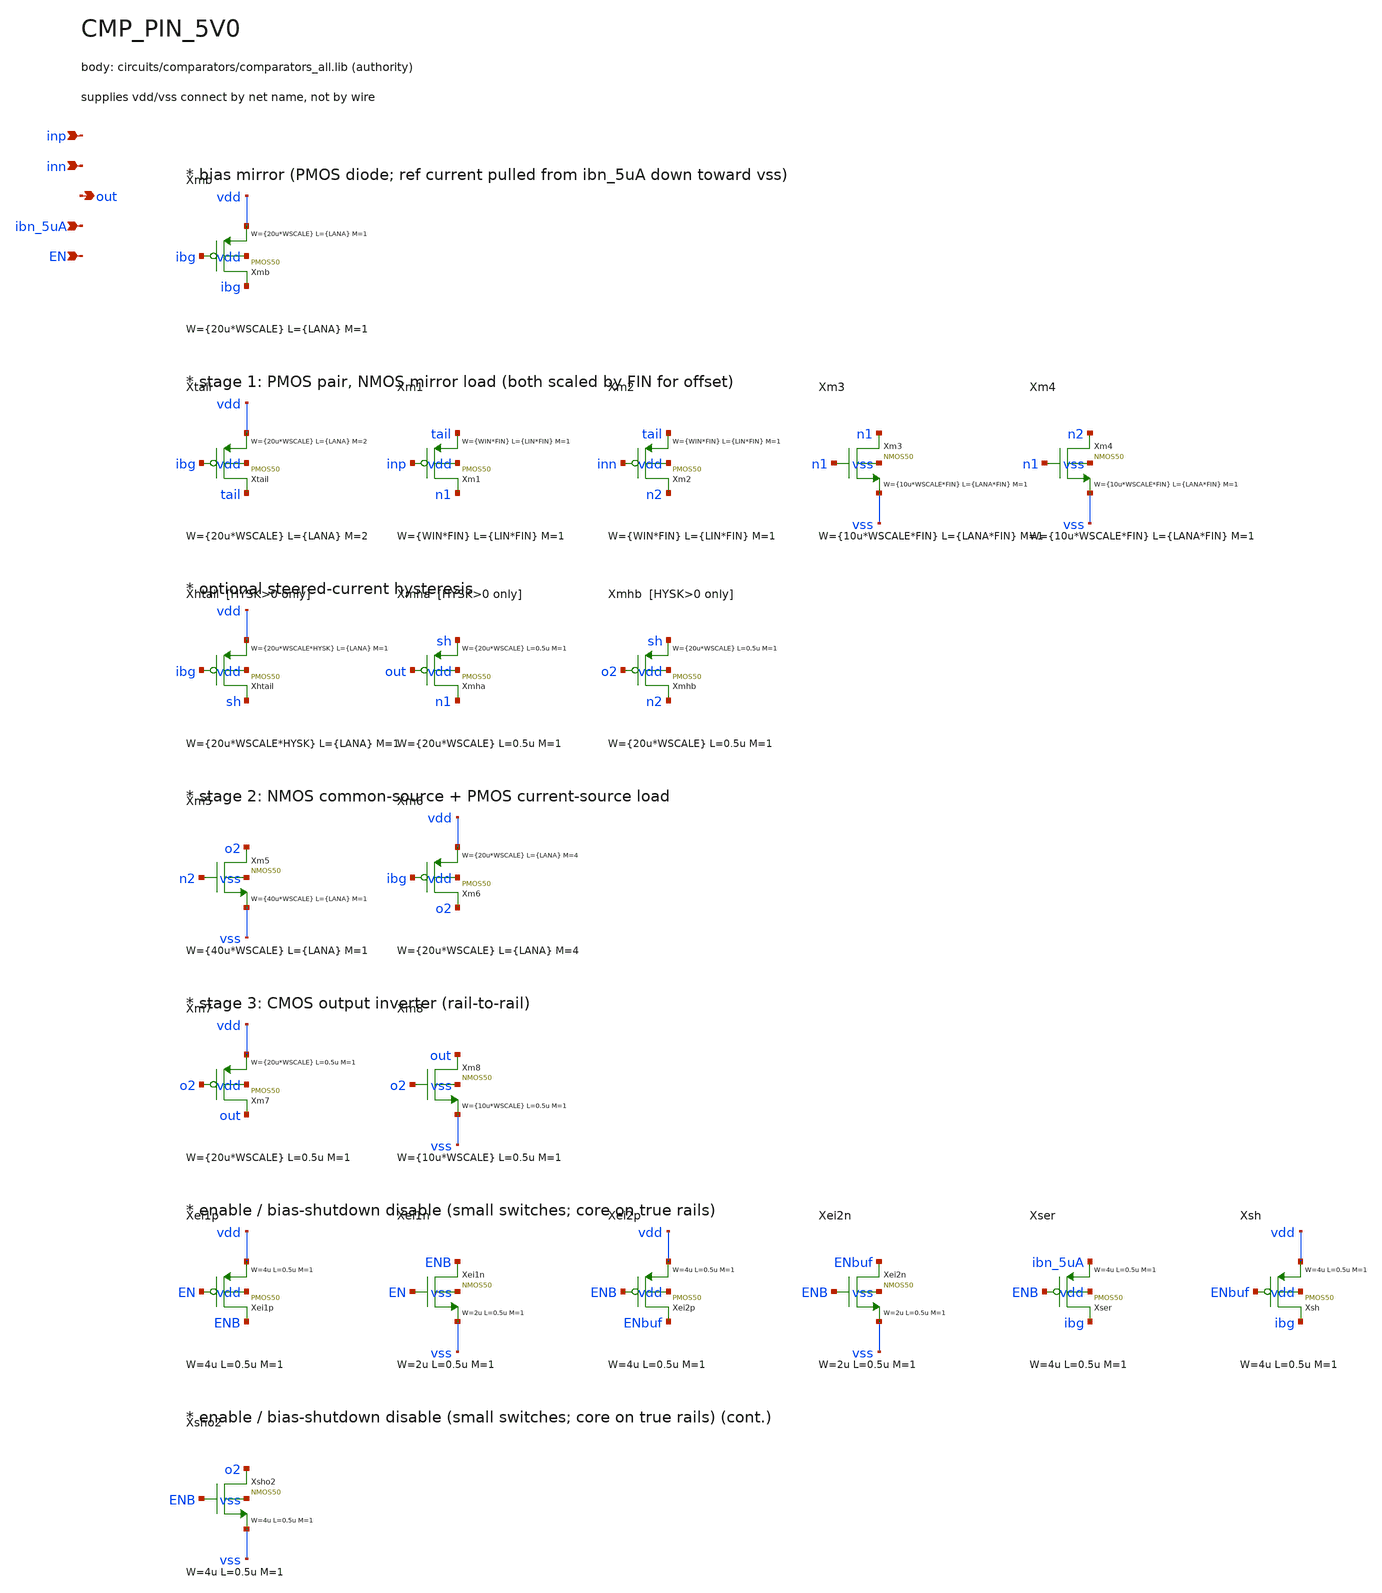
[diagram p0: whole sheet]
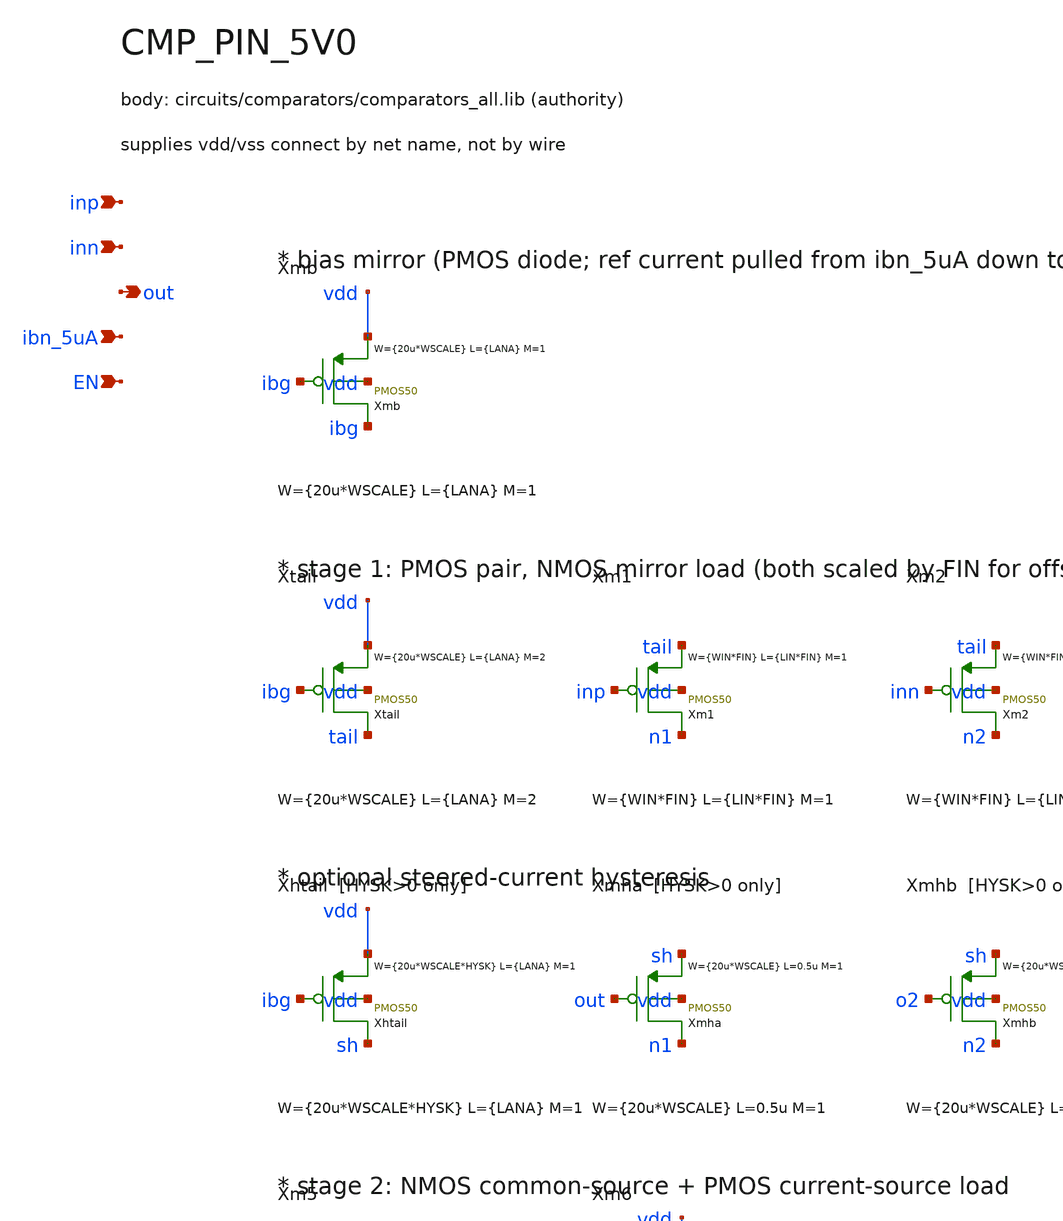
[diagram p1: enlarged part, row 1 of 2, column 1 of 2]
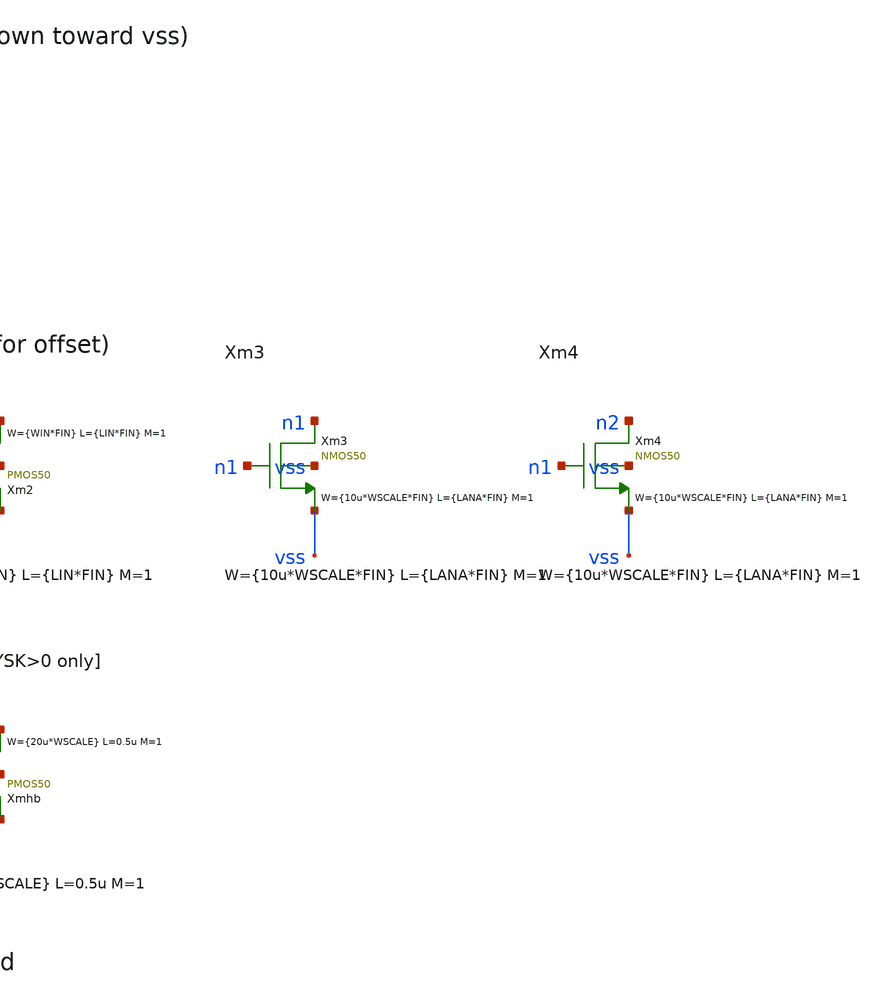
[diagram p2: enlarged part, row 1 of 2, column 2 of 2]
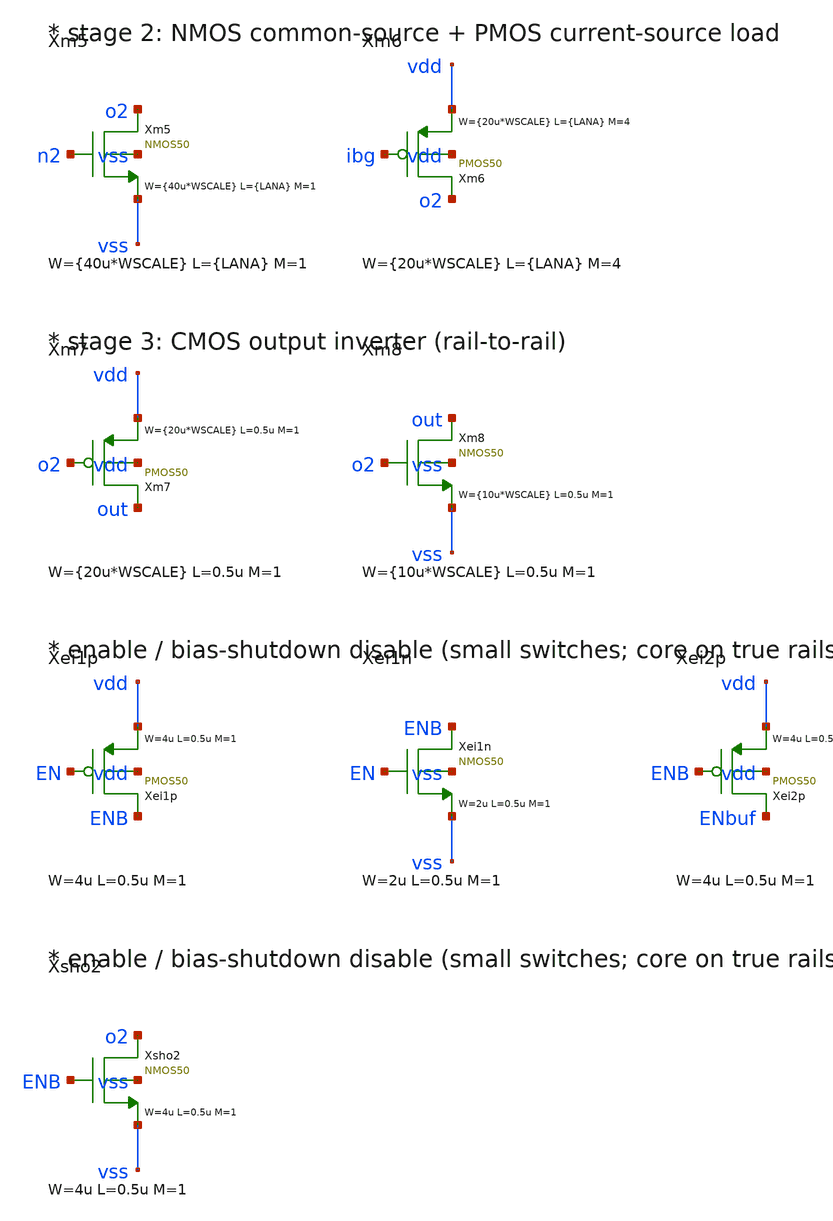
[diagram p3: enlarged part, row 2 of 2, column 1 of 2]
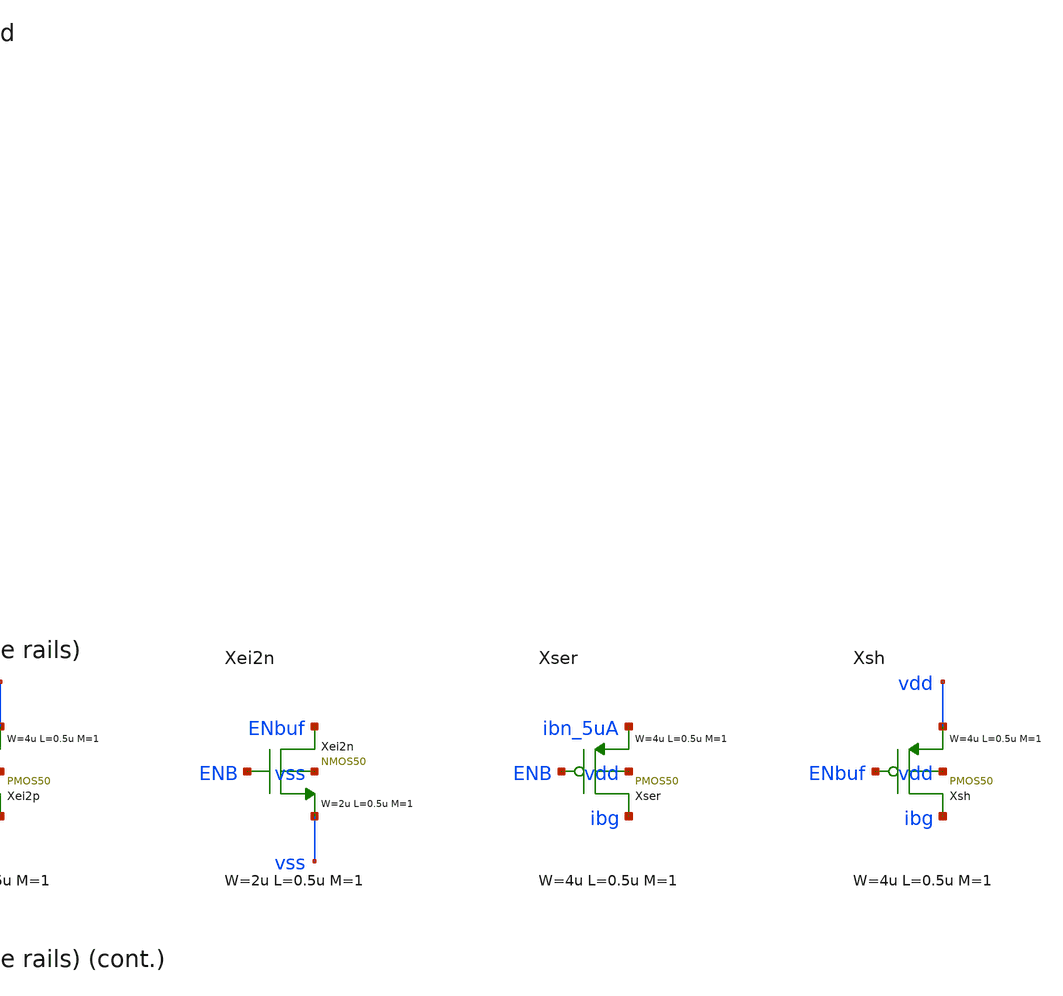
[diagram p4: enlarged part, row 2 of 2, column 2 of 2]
** sch_path: xschem/comparators/CMP_PIN_5V0.sch
**.subckt CMP_PIN_5V0 inp inn out ibn_5uA EN
*.ipin inp
*.ipin inn
*.opin out
*.ipin ibn_5uA
*.ipin EN
Xmb ibg ibg vdd vdd PMOS50 W={20u*WSCALE} L={LANA} M=1 MM_SIGMA=0
Xtail tail ibg vdd vdd PMOS50 W={20u*WSCALE} L={LANA} M=2 MM_SIGMA=0
Xm1 n1 inp tail vdd PMOS50 W={WIN*FIN} L={LIN*FIN} M=1 MM_SIGMA=0
Xm2 n2 inn tail vdd PMOS50 W={WIN*FIN} L={LIN*FIN} M=1 MM_SIGMA=0
Xm3 n1 n1 vss vss NMOS50 W={10u*WSCALE*FIN} L={LANA*FIN} M=1 MM_SIGMA=0
Xm4 n2 n1 vss vss NMOS50 W={10u*WSCALE*FIN} L={LANA*FIN} M=1 MM_SIGMA=0
Xhtail sh ibg vdd vdd PMOS50 W={20u*WSCALE*HYSK} L={LANA} M=1 MM_SIGMA=0
Xmha n1 out sh vdd PMOS50 W={20u*WSCALE} L=0.5u M=1 MM_SIGMA=0
Xmhb n2 o2 sh vdd PMOS50 W={20u*WSCALE} L=0.5u M=1 MM_SIGMA=0
Xm5 o2 n2 vss vss NMOS50 W={40u*WSCALE} L={LANA} M=1 MM_SIGMA=0
Xm6 o2 ibg vdd vdd PMOS50 W={20u*WSCALE} L={LANA} M=4 MM_SIGMA=0
Xm7 out o2 vdd vdd PMOS50 W={20u*WSCALE} L=0.5u M=1 MM_SIGMA=0
Xm8 out o2 vss vss NMOS50 W={10u*WSCALE} L=0.5u M=1 MM_SIGMA=0
Xei1p ENB EN vdd vdd PMOS50 W=4u L=0.5u M=1 MM_SIGMA=0
Xei1n ENB EN vss vss NMOS50 W=2u L=0.5u M=1 MM_SIGMA=0
Xei2p ENbuf ENB vdd vdd PMOS50 W=4u L=0.5u M=1 MM_SIGMA=0
Xei2n ENbuf ENB vss vss NMOS50 W=2u L=0.5u M=1 MM_SIGMA=0
Xser ibg ENB ibn_5uA vdd PMOS50 W=4u L=0.5u M=1 MM_SIGMA=0
Xsh ibg ENbuf vdd vdd PMOS50 W=4u L=0.5u M=1 MM_SIGMA=0
Xsho2 o2 ENB vss vss NMOS50 W=4u L=0.5u M=1 MM_SIGMA=0
**.ends
.end
